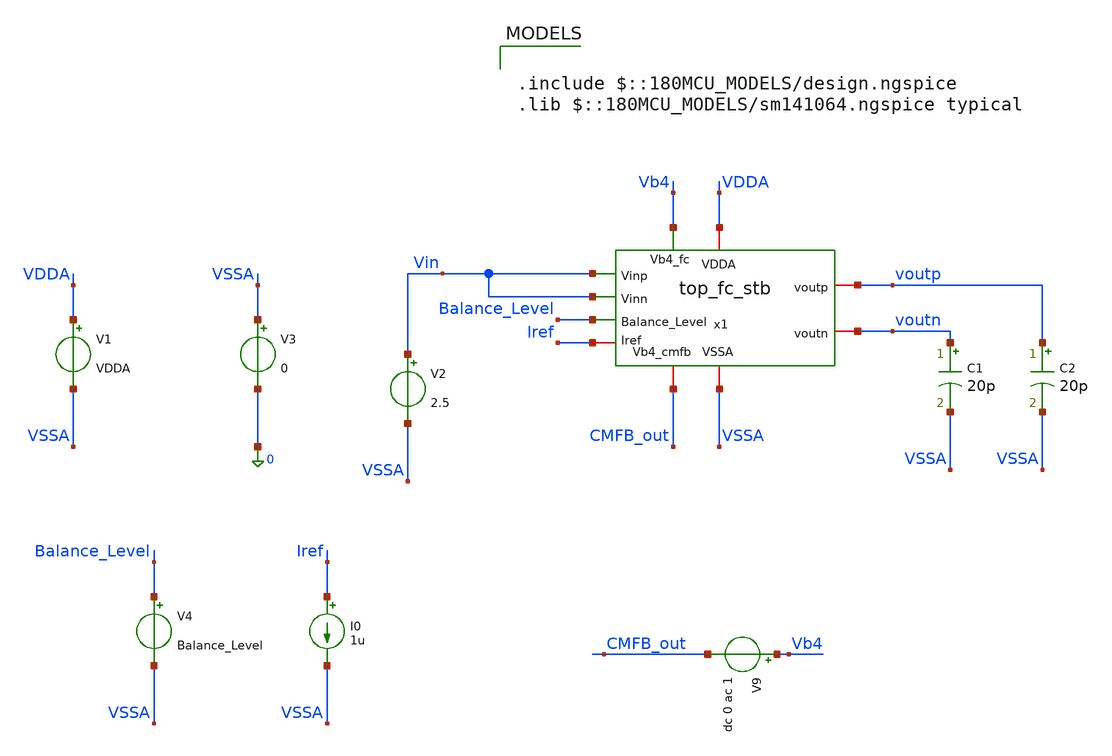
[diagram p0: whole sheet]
** sch_path: Folded_cascode/testbenches/top_fc_stb_tb.sch
**.subckt top_fc_stb_tb
V2 Vin VSSA 2.5
C1 voutn VSSA 20p m=1
C2 voutp VSSA 20p m=1
V1 VDDA VSSA VDDA
V3 VSSA 0 0
V4 Balance_Level VSSA Balance_Level
I0 Iref VSSA 1u
x1 CMFB_out Vb4 Balance_Level Vin voutp VDDA voutn Vin Iref VSSA top_fc_stb
V9 Vb4 CMFB_out dc 0 ac 1
**** begin user architecture code

.include $::180MCU_MODELS/design.ngspice
.lib $::180MCU_MODELS/sm141064.ngspice typical



.temp 27
.param VDDA = 5
.param Balance_Level = 1.5

.control
option sparse
set filetype=ascii
set wr_singlescale
set wr_vecnames
save all
save @m.x1.x1.xm1.m0[id]
save @m.x1.x1.xm1.m0[gm]
save @m.x1.x1.xm1.m0[vgs]
save @m.x1.x1.xm1.m0[vds]
save @m.x1.x1.xm1.m0[vth]
save @m.x1.x1.xm1.m0[gds]
save @m.x1.x1.xm1.m0[vdsat]

save @m.x1.x1.xm2.m0[id]
save @m.x1.x1.xm2.m0[gm]
save @m.x1.x1.xm2.m0[vgs]
save @m.x1.x1.xm2.m0[vds]
save @m.x1.x1.xm2.m0[vth]
save @m.x1.x1.xm2.m0[gds]
save @m.x1.x1.xm2.m0[vdsat]

save @m.x1.x1.xm9.m0[id]
save @m.x1.x1.xm9.m0[gm]
save @m.x1.x1.xm9.m0[vgs]
save @m.x1.x1.xm9.m0[vds]
save @m.x1.x1.xm9.m0[vth]
save @m.x1.x1.xm9.m0[gds]
save @m.x1.x1.xm9.m0[vdsat]

save @m.x1.x1.xm8.m0[id]
save @m.x1.x1.xm8.m0[gm]
save @m.x1.x1.xm8.m0[vgs]
save @m.x1.x1.xm8.m0[vds]
save @m.x1.x1.xm8.m0[vth]
save @m.x1.x1.xm8.m0[gds]
save @m.x1.x1.xm8.m0[vdsat]

save @m.x1.x1.xm6.m0[id]
save @m.x1.x1.xm6.m0[gm]
save @m.x1.x1.xm6.m0[vgs]
save @m.x1.x1.xm6.m0[vds]
save @m.x1.x1.xm6.m0[vth]
save @m.x1.x1.xm6.m0[gds]
save @m.x1.x1.xm6.m0[vdsat]

save @m.x1.x1.xm5.m0[id]
save @m.x1.x1.xm5.m0[gm]
save @m.x1.x1.xm5.m0[vgs]
save @m.x1.x1.xm5.m0[vds]
save @m.x1.x1.xm5.m0[vth]
save @m.x1.x1.xm5.m0[gds]
save @m.x1.x1.xm5.m0[vdsat]

save @m.x1.x2.xm1.m0[id]
save @m.x1.x2.xm1.m0[gm]
save @m.x1.x2.xm1.m0[vgs]
save @m.x1.x2.xm1.m0[vds]
save @m.x1.x2.xm1.m0[vth]
save @m.x1.x2.xm1.m0[gds]

save @m.x1.x2.xm2.m0[id]
save @m.x1.x2.xm2.m0[gm]
save @m.x1.x2.xm2.m0[vgs]
save @m.x1.x2.xm2.m0[vds]
save @m.x1.x2.xm2.m0[vth]
save @m.x1.x2.xm2.m0[gds]

save @m.x1.x2.xm3.m0[id]
save @m.x1.x2.xm3.m0[gm]
save @m.x1.x2.xm3.m0[vgs]
save @m.x1.x2.xm3.m0[vds]
save @m.x1.x2.xm3.m0[vth]
save @m.x1.x2.xm3.m0[gds]

save @m.x1.x2.xm4.m0[id]
save @m.x1.x2.xm4.m0[gm]
save @m.x1.x2.xm4.m0[vgs]
save @m.x1.x2.xm4.m0[vds]
save @m.x1.x2.xm4.m0[vth]
save @m.x1.x2.xm4.m0[gds]

save @m.x1.x2.xm5.m0[id]
save @m.x1.x2.xm5.m0[gm]
save @m.x1.x2.xm5.m0[vgs]
save @m.x1.x2.xm5.m0[vds]
save @m.x1.x2.xm5.m0[vth]
save @m.x1.x2.xm5.m0[gds]

save @m.x1.x2.xm6.m0[id]
save @m.x1.x2.xm6.m0[gm]
save @m.x1.x2.xm6.m0[vgs]
save @m.x1.x2.xm6.m0[vds]
save @m.x1.x2.xm6.m0[vth]
save @m.x1.x2.xm6.m0[gds]

save @m.x1.x2.xm7.m0[id]
save @m.x1.x2.xm7.m0[gm]
save @m.x1.x2.xm7.m0[vgs]
save @m.x1.x2.xm7.m0[vds]
save @m.x1.x2.xm7.m0[vth]
save @m.x1.x2.xm7.m0[gds]

save @m.x1.x2.xm8.m0[id]
save @m.x1.x2.xm8.m0[gm]
save @m.x1.x2.xm8.m0[vgs]
save @m.x1.x2.xm8.m0[vds]
save @m.x1.x2.xm8.m0[vth]
save @m.x1.x2.xm8.m0[gds]

save @m.x1.x2.xm9.m0[id]
save @m.x1.x2.xm9.m0[gm]
save @m.x1.x2.xm9.m0[vgs]
save @m.x1.x2.xm9.m0[vds]
save @m.x1.x2.xm9.m0[vth]
save @m.x1.x2.xm9.m0[gds]

save @m.x1.x3.xm1.m0[id]
save @m.x1.x3.xm1.m0[gm]
save @m.x1.x3.xm1.m0[vgs]
save @m.x1.x3.xm1.m0[vds]
save @m.x1.x3.xm1.m0[vth]
save @m.x1.x3.xm1.m0[gds]

save @m.x1.x3.xm2.m0[id]
save @m.x1.x3.xm2.m0[gm]
save @m.x1.x3.xm2.m0[vgs]
save @m.x1.x3.xm2.m0[vds]
save @m.x1.x3.xm2.m0[vth]
save @m.x1.x3.xm2.m0[gds]

save @m.x1.x3.xm3.m0[id]
save @m.x1.x3.xm3.m0[gm]
save @m.x1.x3.xm3.m0[vgs]
save @m.x1.x3.xm3.m0[vds]
save @m.x1.x3.xm3.m0[vth]
save @m.x1.x3.xm3.m0[gds]

save @m.x1.x3.xm4.m0[id]
save @m.x1.x3.xm4.m0[gm]
save @m.x1.x3.xm4.m0[vgs]
save @m.x1.x3.xm4.m0[vds]
save @m.x1.x3.xm4.m0[vth]
save @m.x1.x3.xm4.m0[gds]

save @m.x1.x3.xm5.m0[id]
save @m.x1.x3.xm5.m0[gm]
save @m.x1.x3.xm5.m0[vgs]
save @m.x1.x3.xm5.m0[vds]
save @m.x1.x3.xm5.m0[vth]
save @m.x1.x3.xm5.m0[gds]

save @m.x1.x3.xm6.m0[id]
save @m.x1.x3.xm6.m0[gm]
save @m.x1.x3.xm6.m0[vgs]
save @m.x1.x3.xm6.m0[vds]
save @m.x1.x3.xm6.m0[vth]
save @m.x1.x3.xm6.m0[gds]

save @m.x1.x3.xm7.m0[id]
save @m.x1.x3.xm7.m0[gm]
save @m.x1.x3.xm7.m0[vgs]
save @m.x1.x3.xm7.m0[vds]
save @m.x1.x3.xm7.m0[vth]
save @m.x1.x3.xm7.m0[gds]

save @m.x1.x3.xm8.m0[id]
save @m.x1.x3.xm8.m0[gm]
save @m.x1.x3.xm8.m0[vgs]
save @m.x1.x3.xm8.m0[vds]
save @m.x1.x3.xm8.m0[vth]
save @m.x1.x3.xm8.m0[gds]

save @m.x1.x3.xm9.m0[id]
save @m.x1.x3.xm9.m0[gm]
save @m.x1.x3.xm9.m0[vgs]
save @m.x1.x3.xm9.m0[vds]
save @m.x1.x3.xm9.m0[vth]
save @m.x1.x3.xm9.m0[gds]

save @m.x1.x3.xm10.m0[id]
save @m.x1.x3.xm10.m0[gm]
save @m.x1.x3.xm10.m0[vgs]
save @m.x1.x3.xm10.m0[vds]
save @m.x1.x3.xm10.m0[vth]
save @m.x1.x3.xm10.m0[gds]

save @m.x1.x3.xm11.m0[id]
save @m.x1.x3.xm11.m0[gm]
save @m.x1.x3.xm11.m0[vgs]
save @m.x1.x3.xm11.m0[vds]
save @m.x1.x3.xm11.m0[vth]
save @m.x1.x3.xm11.m0[gds]

save @m.x1.x3.xm12.m0[id]
save @m.x1.x3.xm12.m0[gm]
save @m.x1.x3.xm12.m0[vgs]
save @m.x1.x3.xm12.m0[vds]
save @m.x1.x3.xm12.m0[vth]
save @m.x1.x3.xm12.m0[gds]

save @m.x1.x3.xm13.m0[id]
save @m.x1.x3.xm13.m0[gm]
save @m.x1.x3.xm13.m0[vgs]
save @m.x1.x3.xm13.m0[vds]
save @m.x1.x3.xm13.m0[vth]
save @m.x1.x3.xm13.m0[gds]

save @m.x1.x3.xm14.m0[id]
save @m.x1.x3.xm14.m0[gm]
save @m.x1.x3.xm14.m0[vgs]
save @m.x1.x3.xm14.m0[vds]
save @m.x1.x3.xm14.m0[vth]
save @m.x1.x3.xm14.m0[gds]

save @m.x1.x3.xm15.m0[id]
save @m.x1.x3.xm15.m0[gm]
save @m.x1.x3.xm15.m0[vgs]
save @m.x1.x3.xm15.m0[vds]
save @m.x1.x3.xm15.m0[vth]
save @m.x1.x3.xm15.m0[gds]

save @m.x1.x3.xm16.m0[id]
save @m.x1.x3.xm16.m0[gm]
save @m.x1.x3.xm16.m0[vgs]
save @m.x1.x3.xm16.m0[vds]
save @m.x1.x3.xm16.m0[vth]
save @m.x1.x3.xm16.m0[gds]

save @m.x1.x3.xm17.m0[id]
save @m.x1.x3.xm17.m0[gm]
save @m.x1.x3.xm17.m0[vgs]
save @m.x1.x3.xm17.m0[vds]
save @m.x1.x3.xm17.m0[vth]
save @m.x1.x3.xm17.m0[gds]

save @m.x1.x3.xm18.m0[id]
save @m.x1.x3.xm18.m0[gm]
save @m.x1.x3.xm18.m0[vgs]
save @m.x1.x3.xm18.m0[vds]
save @m.x1.x3.xm18.m0[vth]
save @m.x1.x3.xm18.m0[gds]

save @m.x1.x3.xm21.m0[id]
save @m.x1.x3.xm21.m0[gm]
save @m.x1.x3.xm21.m0[vgs]
save @m.x1.x3.xm21.m0[vds]
save @m.x1.x3.xm21.m0[vth]
save @m.x1.x3.xm21.m0[gds]

save @m.x1.x3.xm22.m0[id]
save @m.x1.x3.xm22.m0[gm]
save @m.x1.x3.xm22.m0[vgs]
save @m.x1.x3.xm22.m0[vds]
save @m.x1.x3.xm22.m0[vth]
save @m.x1.x3.xm22.m0[gds]

op
write top_fc_op_tb.raw all

set appendwrite
ac dec 100 1 1G

* Approximate CMFB loop gain
let loopgain = -v(CMFB_out)/v(Vb4)

* Magnitude and phase in degrees
let lg_db = db(loopgain)
let lg_phase_deg = phase(loopgain)*180/3.141592653589793

* -------------------------------------------------
* First 0-dB crossing
* -------------------------------------------------
meas ac f_ugf1 WHEN lg_db=0 CROSS=1
meas ac phase_ugf1 FIND lg_phase_deg AT=$&f_ugf1

let pm1 = 180 + phase_ugf1

* -------------------------------------------------
* Second 0-dB crossing
* -------------------------------------------------
meas ac f_ugf2 WHEN lg_db=0 CROSS=2
meas ac phase_ugf2 FIND lg_phase_deg AT=$&f_ugf2

* phase() wraps the phase between approximately -180 and +180 deg.
* At the second crossing, convert the positive wrapped phase
* to its continuous negative equivalent.
let phase_ugf2_unwrapped = phase_ugf2 - 360
let pm2 = 180 + phase_ugf2_unwrapped

* -------------------------------------------------
* Results
* -------------------------------------------------
print f_ugf1
print phase_ugf1
print pm1

print f_ugf2
print phase_ugf2
print phase_ugf2_unwrapped
print pm2

write top_fc_stb_tb.raw

plot lg_db
plot lg_phase_deg

.endc


**** end user architecture code
**.ends
.end
